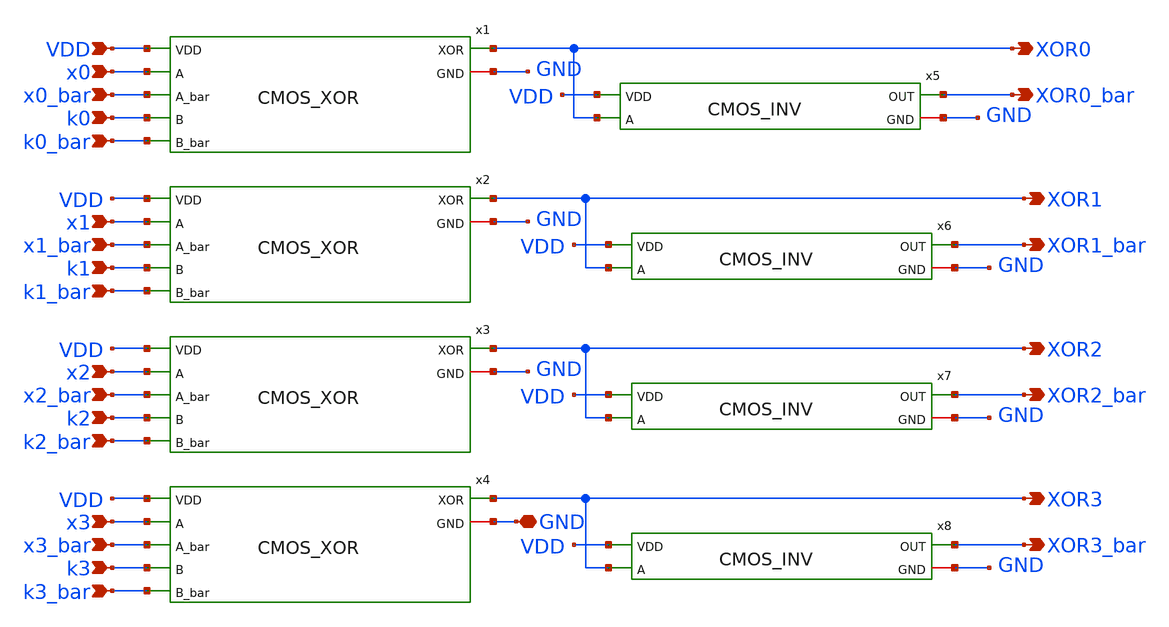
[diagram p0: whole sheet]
** sch_path: skywater_stuff/CMOS_4in_XOR.sch
**.subckt CMOS_4in_XOR x0 x0_bar x1 x1_bar x2 x2_bar x3 x3_bar VDD GND XOR0 XOR1 XOR2 XOR3 k0 k0_bar
*+ k1 k1_bar k2 k2_bar k3 k3_bar XOR0_bar XOR1_bar XOR2_bar XOR3_bar
*.ipin x0
*.ipin x0_bar
*.ipin x1
*.ipin x1_bar
*.ipin x2
*.ipin x2_bar
*.ipin x3
*.ipin x3_bar
*.ipin VDD
*.iopin GND
*.opin XOR0
*.opin XOR1
*.opin XOR2
*.opin XOR3
*.ipin k0
*.ipin k0_bar
*.ipin k1
*.ipin k1_bar
*.ipin k2
*.ipin k2_bar
*.ipin k3
*.ipin k3_bar
*.opin XOR0_bar
*.opin XOR1_bar
*.opin XOR2_bar
*.opin XOR3_bar
x1 x0 x0_bar k0 k0_bar XOR0 GND VDD CMOS_XOR
x2 x1 x1_bar k1 k1_bar XOR1 GND VDD CMOS_XOR
x3 x2 x2_bar k2 k2_bar XOR2 GND VDD CMOS_XOR
x4 x3 x3_bar k3 k3_bar XOR3 GND VDD CMOS_XOR
x5 VDD XOR0 XOR0_bar GND CMOS_INV
x6 VDD XOR1 XOR1_bar GND CMOS_INV
x7 VDD XOR2 XOR2_bar GND CMOS_INV
x8 VDD XOR3 XOR3_bar GND CMOS_INV
**.ends

* expanding   symbol:  CMOS_XOR.sym # of pins=7
** sym_path: skywater_stuff/CMOS_XOR.sym
** sch_path: skywater_stuff/CMOS_XOR.sch
.subckt CMOS_XOR A A_bar B B_bar XOR GND VDD
*.ipin A
*.ipin A_bar
*.ipin B
*.ipin B_bar
*.opin XOR
*.iopin GND
*.ipin VDD
XM8 net4 A_bar GND GND sky130_fd_pr__nfet_01v8 L=0.15 W=1.5 nf=1 ad='int((nf+1)/2) * W/nf * 0.29' as='int((nf+2)/2) * W/nf * 0.29'
+ pd='2*int((nf+1)/2) * (W/nf + 0.29)' ps='2*int((nf+2)/2) * (W/nf + 0.29)' nrd='0.29 / W' nrs='0.29 / W'
+ sa=0 sb=0 sd=0 mult=1 m=1
XM1 XOR B net3 GND sky130_fd_pr__nfet_01v8 L=0.15 W=1.5 nf=1 ad='int((nf+1)/2) * W/nf * 0.29' as='int((nf+2)/2) * W/nf * 0.29'
+ pd='2*int((nf+1)/2) * (W/nf + 0.29)' ps='2*int((nf+2)/2) * (W/nf + 0.29)' nrd='0.29 / W' nrs='0.29 / W'
+ sa=0 sb=0 sd=0 mult=1 m=1
XM3 XOR A net1 VDD sky130_fd_pr__pfet_01v8 L=0.15 W=3 nf=1 ad='int((nf+1)/2) * W/nf * 0.29' as='int((nf+2)/2) * W/nf * 0.29'
+ pd='2*int((nf+1)/2) * (W/nf + 0.29)' ps='2*int((nf+2)/2) * (W/nf + 0.29)' nrd='0.29 / W' nrs='0.29 / W'
+ sa=0 sb=0 sd=0 mult=1 m=1
XM4 net2 B VDD VDD sky130_fd_pr__pfet_01v8 L=0.15 W=3 nf=1 ad='int((nf+1)/2) * W/nf * 0.29' as='int((nf+2)/2) * W/nf * 0.29'
+ pd='2*int((nf+1)/2) * (W/nf + 0.29)' ps='2*int((nf+2)/2) * (W/nf + 0.29)' nrd='0.29 / W' nrs='0.29 / W'
+ sa=0 sb=0 sd=0 mult=1 m=1
XM9 net1 B_bar VDD VDD sky130_fd_pr__pfet_01v8 L=0.15 W=3 nf=1 ad='int((nf+1)/2) * W/nf * 0.29' as='int((nf+2)/2) * W/nf * 0.29'
+ pd='2*int((nf+1)/2) * (W/nf + 0.29)' ps='2*int((nf+2)/2) * (W/nf + 0.29)' nrd='0.29 / W' nrs='0.29 / W'
+ sa=0 sb=0 sd=0 mult=1 m=1
XM2 XOR B_bar net4 GND sky130_fd_pr__nfet_01v8 L=0.15 W=1.5 nf=1 ad='int((nf+1)/2) * W/nf * 0.29' as='int((nf+2)/2) * W/nf * 0.29'
+ pd='2*int((nf+1)/2) * (W/nf + 0.29)' ps='2*int((nf+2)/2) * (W/nf + 0.29)' nrd='0.29 / W' nrs='0.29 / W'
+ sa=0 sb=0 sd=0 mult=1 m=1
XM5 net3 A GND GND sky130_fd_pr__nfet_01v8 L=0.15 W=1.5 nf=1 ad='int((nf+1)/2) * W/nf * 0.29' as='int((nf+2)/2) * W/nf * 0.29'
+ pd='2*int((nf+1)/2) * (W/nf + 0.29)' ps='2*int((nf+2)/2) * (W/nf + 0.29)' nrd='0.29 / W' nrs='0.29 / W'
+ sa=0 sb=0 sd=0 mult=1 m=1
XM10 XOR A_bar net2 VDD sky130_fd_pr__pfet_01v8 L=0.15 W=3 nf=1 ad='int((nf+1)/2) * W/nf * 0.29' as='int((nf+2)/2) * W/nf * 0.29'
+ pd='2*int((nf+1)/2) * (W/nf + 0.29)' ps='2*int((nf+2)/2) * (W/nf + 0.29)' nrd='0.29 / W' nrs='0.29 / W'
+ sa=0 sb=0 sd=0 mult=1 m=1
.ends


* expanding   symbol:  CMOS_INV.sym # of pins=4
** sym_path: skywater_stuff/CMOS_INV.sym
** sch_path: skywater_stuff/CMOS_INV.sch
.subckt CMOS_INV VDD A OUT GND
*.iopin GND
*.ipin A
*.ipin VDD
*.opin OUT
XM1 OUT A VDD VDD sky130_fd_pr__pfet_01v8 L=0.15 W=3 nf=1 ad='int((nf+1)/2) * W/nf * 0.29' as='int((nf+2)/2) * W/nf * 0.29'
+ pd='2*int((nf+1)/2) * (W/nf + 0.29)' ps='2*int((nf+2)/2) * (W/nf + 0.29)' nrd='0.29 / W' nrs='0.29 / W'
+ sa=0 sb=0 sd=0 mult=1 m=1
XM2 OUT A GND GND sky130_fd_pr__nfet_01v8 L=0.15 W=1.5 nf=1 ad='int((nf+1)/2) * W/nf * 0.29' as='int((nf+2)/2) * W/nf * 0.29'
+ pd='2*int((nf+1)/2) * (W/nf + 0.29)' ps='2*int((nf+2)/2) * (W/nf + 0.29)' nrd='0.29 / W' nrs='0.29 / W'
+ sa=0 sb=0 sd=0 mult=1 m=1
.ends

.end
